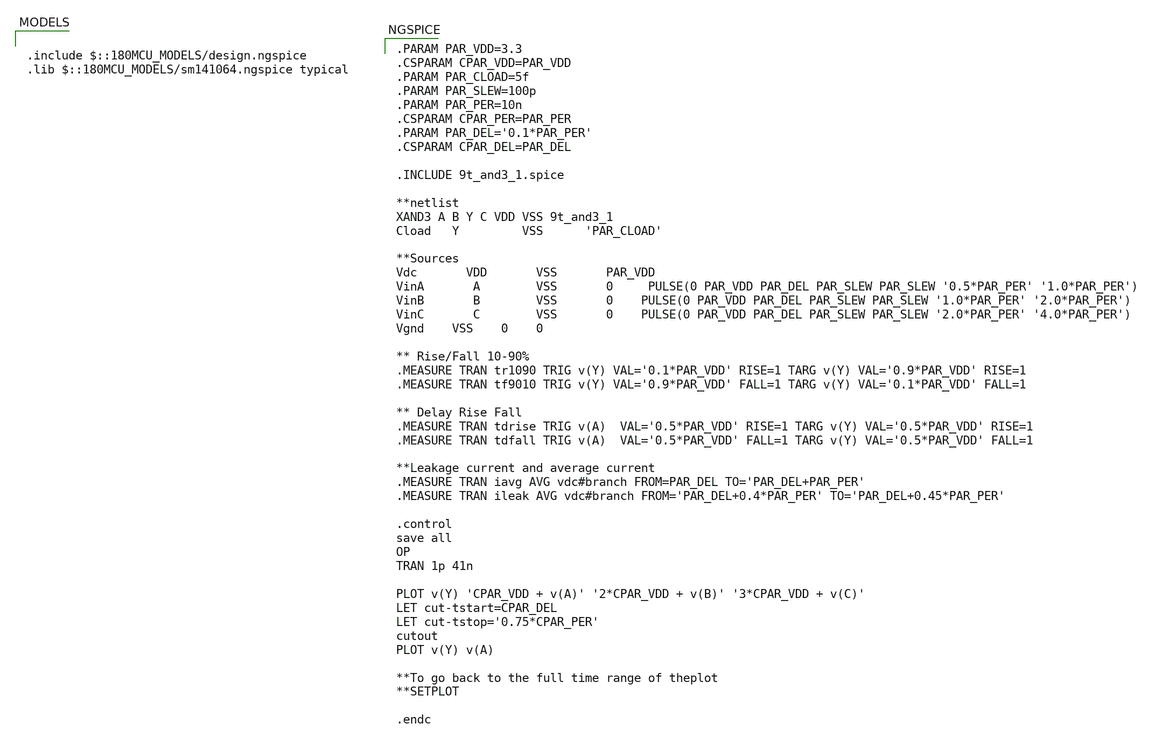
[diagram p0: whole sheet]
** sch_path: 9t_and3_1/tb_9t_and3_1.sch
**.subckt tb_9t_and3_1
**** begin user architecture code

.PARAM PAR_VDD=3.3
.CSPARAM CPAR_VDD=PAR_VDD
.PARAM PAR_CLOAD=5f
.PARAM PAR_SLEW=100p
.PARAM PAR_PER=10n
.CSPARAM CPAR_PER=PAR_PER
.PARAM PAR_DEL='0.1*PAR_PER'
.CSPARAM CPAR_DEL=PAR_DEL

.INCLUDE 9t_and3_1.spice

**netlist
XAND3 A B Y C VDD VSS 9t_and3_1
Cload   Y     	VSS  	'PAR_CLOAD'

**Sources
Vdc   	VDD   	VSS   	PAR_VDD
VinA   	A    	VSS   	0 	PULSE(0 PAR_VDD PAR_DEL PAR_SLEW PAR_SLEW '0.5*PAR_PER' '1.0*PAR_PER')
VinB   	B    	VSS   	0	PULSE(0 PAR_VDD PAR_DEL PAR_SLEW PAR_SLEW '1.0*PAR_PER' '2.0*PAR_PER')
VinC   	C    	VSS   	0	PULSE(0 PAR_VDD PAR_DEL PAR_SLEW PAR_SLEW '2.0*PAR_PER' '4.0*PAR_PER')
Vgnd	VSS	0	0

** Rise/Fall 10-90%
.MEASURE TRAN tr1090 TRIG v(Y) VAL='0.1*PAR_VDD' RISE=1 TARG v(Y) VAL='0.9*PAR_VDD' RISE=1
.MEASURE TRAN tf9010 TRIG v(Y) VAL='0.9*PAR_VDD' FALL=1 TARG v(Y) VAL='0.1*PAR_VDD' FALL=1

** Delay Rise Fall
.MEASURE TRAN tdrise TRIG v(A)  VAL='0.5*PAR_VDD' RISE=1 TARG v(Y) VAL='0.5*PAR_VDD' RISE=1
.MEASURE TRAN tdfall TRIG v(A)  VAL='0.5*PAR_VDD' FALL=1 TARG v(Y) VAL='0.5*PAR_VDD' FALL=1

**Leakage current and average current
.MEASURE TRAN iavg AVG vdc#branch FROM=PAR_DEL TO='PAR_DEL+PAR_PER'
.MEASURE TRAN ileak AVG vdc#branch FROM='PAR_DEL+0.4*PAR_PER' TO='PAR_DEL+0.45*PAR_PER'

.control
save all
OP
TRAN 1p 41n

PLOT v(Y) 'CPAR_VDD + v(A)' '2*CPAR_VDD + v(B)' '3*CPAR_VDD + v(C)'
LET cut-tstart=CPAR_DEL
LET cut-tstop='0.75*CPAR_PER'
cutout
PLOT v(Y) v(A)

**To go back to the full time range of theplot
**SETPLOT

.endc


.include $::180MCU_MODELS/design.ngspice
.lib $::180MCU_MODELS/sm141064.ngspice typical

**** end user architecture code
**.ends
.end
